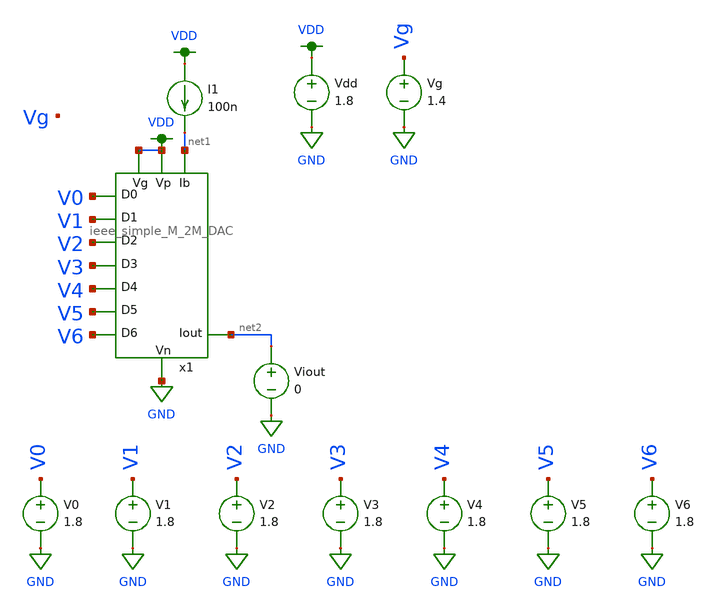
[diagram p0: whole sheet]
** sch_path: schematics/ieee_DAC_mc_simulation.sch
**.subckt ieee_DAC_mc_simulation
I1 VDD net1 100n
Vdd VDD GND 1.8
V1 V1 GND 1.8
V2 V2 GND 1.8
V3 V3 GND 1.8
V4 V4 GND 1.8
V5 V5 GND 1.8
V6 V6 GND 1.8
V0 V0 GND 1.8
Vg Vg GND 1.4
Viout net2 GND 0
x1 VDD net2 GND V1 V0 V2 V3 V4 V5 V6 VDD net1 ieee_simple_M_2M_DAC
**** begin user architecture code

.option wnflag=1
.param MC_SWITCH=0.0
.lib ~/skywater/skywater-pdk/libraries/sky130_fd_pr_ngspice/latest/models/sky130.lib.spice tt



.control
set wr_vecnames
set wr_singlescale

let mc_runs = 1
let run = 1
dowhile run <= mc_runs

  let code = 0
  while code < 128
    if floor(code / 1) eq 0
      let b0 = 0
    else
      let b0 = (floor(code / 1) % 2) * 1.8
    end
    if floor(code / 2) eq 0
      let b1 = 0
    else
      let b1 = (floor(code / 2) % 2) * 1.8
    end
    if floor(code / 4) eq 0
      let b2 = 0
    else
      let b2 = (floor(code / 4) % 2) * 1.8
    end
    if floor(code / 8) eq 0
      let b3 = 0
    else
      let b3 = (floor(code / 8) % 2) * 1.8
    end
    if floor(code / 16) eq 0
      let b4 = 0
    else
      let b4 = (floor(code / 16) % 2) * 1.8
    end
    if floor(code / 32) eq 0
      let b5 = 0
    else
      let b5 = (floor(code / 32) % 2) * 1.8
    end
    if floor(code / 64) eq 0
      let b6 = 0
    else
      let b6 = (floor(code / 64) % 2) * 1.8
    end

    alter V0 $&b0
    alter V1 $&b1
    alter V2 $&b2
    alter V3 $&b3
    alter V4 $&b4
    alter V5 $&b5
    alter V6 $&b6
    op
    save all

    wrdata ~/dev/git/7-bit-D-A-converter-MP4-MADVLSI/schematics/simulations/ieee_DAC/simulation_results/ieee_DAC_{$&run}.txt
+ V0 V1 V2 V3 V4 V5 V6 i(Viout)
    if code eq 0
      set appendwrite
      set wr_vecnames = FALSE
    end
    reset
    let code = code + 1
  end

  set appendwrite = FALSE
  set wr_vecnames
  let run = run + 1
end
quit
.endc

**** end user architecture code
**.ends
.GLOBAL VDD
.GLOBAL GND
.end
